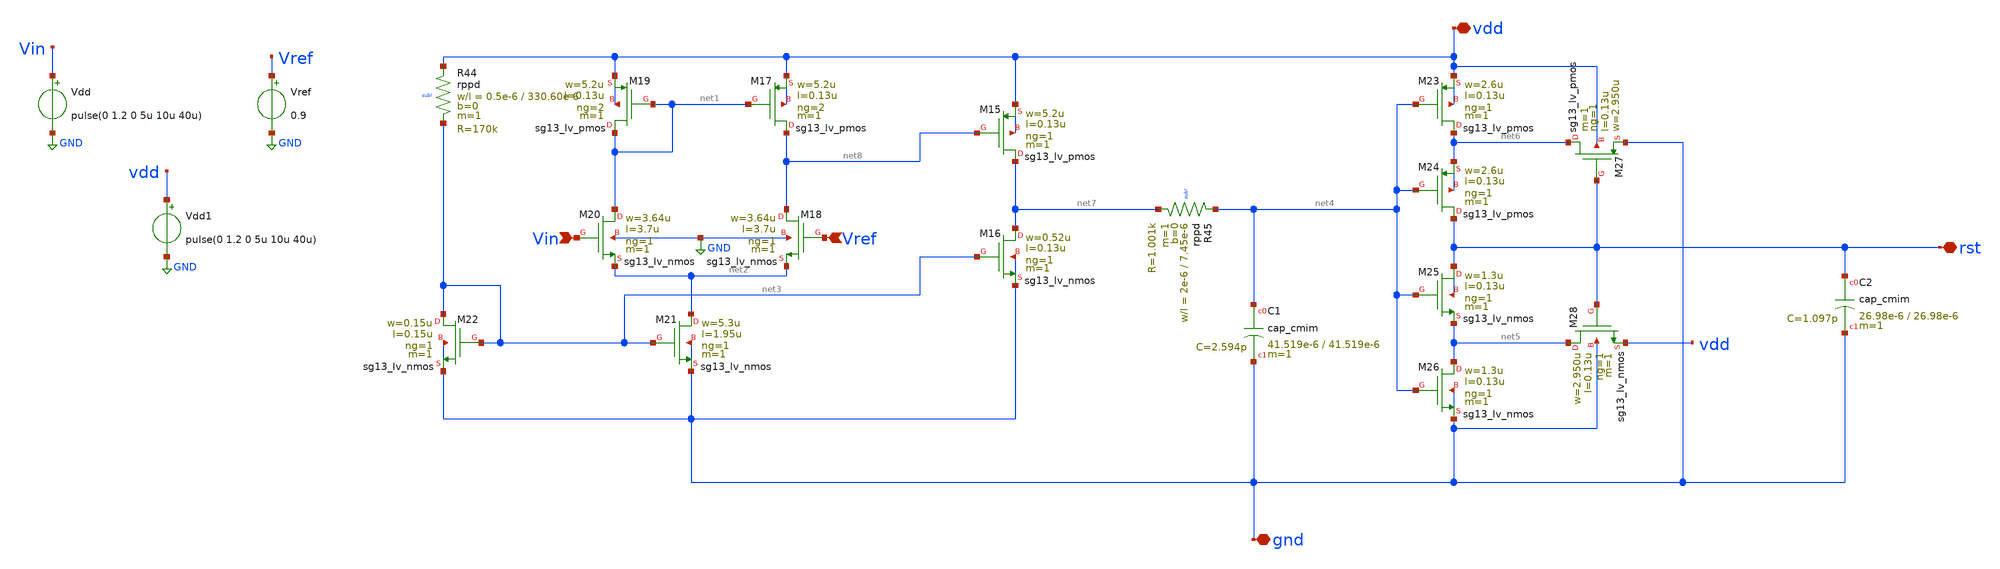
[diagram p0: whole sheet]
** sch_path: dependencies/POR/POR-main/schematic/xschem/POR_sch.sch
**.subckt POR_sch vdd gnd Vin Vref rst
*.iopin vdd
*.iopin gnd
*.ipin Vin
*.ipin Vref
*.iopin rst
XM15 net7 net8 vdd vdd sg13_lv_pmos w=5.2u l=0.13u ng=1 m=1 mm_ok=1
XM16 net7 net3 gnd gnd sg13_lv_nmos w=0.52u l=0.13u ng=1 m=1 mm_ok=1
XM17 net8 net1 vdd vdd sg13_lv_pmos w=5.2u l=0.13u ng=2 m=1 mm_ok=1
XM18 net8 Vref net2 GND sg13_lv_nmos w=3.64u l=3.7u ng=1 m=1 mm_ok=1
XM19 net1 net1 vdd vdd sg13_lv_pmos w=5.2u l=0.13u ng=2 m=1 mm_ok=1
XM20 net1 Vin net2 GND sg13_lv_nmos w=3.64u l=3.7u ng=1 m=1 mm_ok=1
XM21 net2 net3 gnd gnd sg13_lv_nmos w=5.3u l=1.95u ng=1 m=1 mm_ok=1
XM22 net3 net3 gnd gnd sg13_lv_nmos w=0.15u l=0.15u ng=1 m=1 mm_ok=1
XM23 net6 net4 vdd vdd sg13_lv_pmos w=2.6u l=0.13u ng=1 m=1 mm_ok=1
XM24 rst net4 net6 net6 sg13_lv_pmos w=2.6u l=0.13u ng=1 m=1 mm_ok=1
XM25 rst net4 net5 rst sg13_lv_nmos w=1.3u l=0.13u ng=1 m=1 mm_ok=1
XM26 net5 net4 gnd gnd sg13_lv_nmos w=1.3u l=0.13u ng=1 m=1 mm_ok=1
XM27 net6 rst gnd vdd sg13_lv_pmos w=2.950u l=0.13u ng=1 m=1 mm_ok=1
XM28 net5 rst vdd gnd sg13_lv_nmos w=2.950u l=0.13u ng=1 m=1 mm_ok=1
XR44 vdd net3 sub! rppd w=0.5e-6 l=330.60e-6 m=1 b=0 mm_ok=1
XC2 rst gnd cap_cmim w=26.98e-6 l=26.98e-6 m=1 mm_ok=1
XC1 net4 gnd cap_cmim w=41.519e-6 l=41.519e-6 m=1 mm_ok=1
XR45 net4 net7 sub! rppd w=2e-6 l=7.45e-6 m=1 b=0 mm_ok=1
Vref Vref GND 0.9
Vdd Vin GND pulse(0 1.2 0 5u 10u 40u)
Vdd1 vdd GND pulse(0 1.2 0 5u 10u 40u)
**** begin user architecture code


.control
.save all

tran 2n 80u
plot rst vdd


.endc




** IHP models
.lib cornerMOSlv.lib mos_tt
.lib cornerHBT.lib hbt_typ
.lib cornerRES.lib res_typ
.lib cornerCAP.lib cap_typ
.include sg13g2_stdcell.spice


**** end user architecture code
**.ends
.GLOBAL GND
.end
